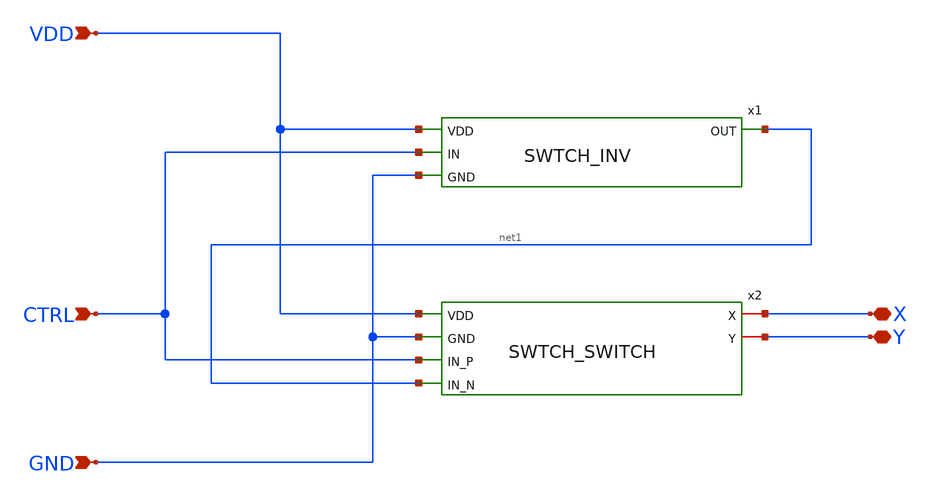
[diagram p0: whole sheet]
** sch_path: swtch_unit_sky130nm/design/SWTCH_UNIT_SKY130NM/SWTCH_UNIT.sch
**.subckt SWTCH_UNIT VDD CTRL GND X Y
*.ipin VDD
*.ipin CTRL
*.ipin GND
*.iopin X
*.iopin Y
x1 VDD CTRL net1 GND SWTCH_INV
x2 VDD GND X CTRL net1 Y SWTCH_SWITCH
**.ends

* expanding   symbol:
*+  /home/couch/dev/personal/chacha-silicon/tt09-analog-switch/swtch_inv_sky130nm/design/SWTCH_INV_SKY130NM/SWTCH_INV.sym # of pins=4
** sym_path: swtch_inv_sky130nm/design/SWTCH_INV_SKY130NM/SWTCH_INV.sym
** sch_path: swtch_inv_sky130nm/design/SWTCH_INV_SKY130NM/SWTCH_INV.sch
.subckt SWTCH_INV VDD IN OUT GND
*.ipin VDD
*.ipin GND
*.ipin IN
*.opin OUT
XM1 OUT IN GND GND sky130_fd_pr__nfet_01v8 L=0.15 W=1 nf=1 ad='int((nf+1)/2) * W/nf * 0.29' as='int((nf+2)/2) * W/nf * 0.29'
+ pd='2*int((nf+1)/2) * (W/nf + 0.29)' ps='2*int((nf+2)/2) * (W/nf + 0.29)' nrd='0.29 / W' nrs='0.29 / W'
+ sa=0 sb=0 sd=0 mult=1 m=1
XM2 OUT IN VDD VDD sky130_fd_pr__pfet_01v8 L=0.15 W=1 nf=1 ad='int((nf+1)/2) * W/nf * 0.29' as='int((nf+2)/2) * W/nf * 0.29'
+ pd='2*int((nf+1)/2) * (W/nf + 0.29)' ps='2*int((nf+2)/2) * (W/nf + 0.29)' nrd='0.29 / W' nrs='0.29 / W'
+ sa=0 sb=0 sd=0 mult=1 m=1
.ends


* expanding   symbol:
*+  /home/couch/dev/personal/chacha-silicon/tt09-analog-switch/swtch_switch_sky130nm/design/SWTCH_SWITCH_SKY130NM/SWTCH_SWITCH.sym # of pins=6
** sym_path: swtch_switch_sky130nm/design/SWTCH_SWITCH_SKY130NM/SWTCH_SWITCH.sym
** sch_path: swtch_switch_sky130nm/design/SWTCH_SWITCH_SKY130NM/SWTCH_SWITCH.sch
.subckt SWTCH_SWITCH VDD GND X IN_P IN_N Y
*.ipin IN_N
*.iopin Y
*.ipin IN_P
*.iopin X
*.ipin VDD
*.ipin GND
XM1 X IN_P Y VDD sky130_fd_pr__pfet_01v8 L=0.36 W=3.6 nf=2 ad='int((nf+1)/2) * W/nf * 0.29' as='int((nf+2)/2) * W/nf * 0.29'
+ pd='2*int((nf+1)/2) * (W/nf + 0.29)' ps='2*int((nf+2)/2) * (W/nf + 0.29)' nrd='0.29 / W' nrs='0.29 / W'
+ sa=0 sb=0 sd=0 mult=1 m=1
XM2 X IN_N Y GND sky130_fd_pr__nfet_01v8 L=0.36 W=3.6 nf=2 ad='int((nf+1)/2) * W/nf * 0.29' as='int((nf+2)/2) * W/nf * 0.29'
+ pd='2*int((nf+1)/2) * (W/nf + 0.29)' ps='2*int((nf+2)/2) * (W/nf + 0.29)' nrd='0.29 / W' nrs='0.29 / W'
+ sa=0 sb=0 sd=0 mult=1 m=1
.ends

.end
